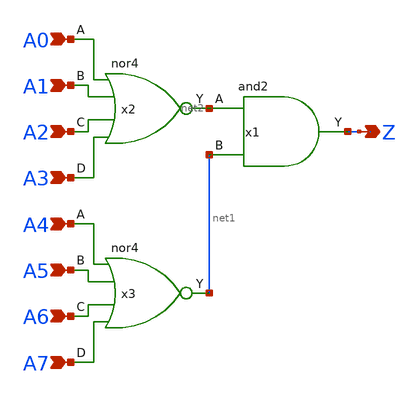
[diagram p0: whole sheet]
** sch_path: design/xschem/ZV_FLAG/Z_FLAG.sch
**.subckt Z_FLAG A0 A1 A2 A3 A4 A5 A6 A7 Z
*.ipin A0
*.ipin A1
*.ipin A2
*.ipin A3
*.ipin A4
*.ipin A5
*.ipin A6
*.ipin A7
*.opin Z
x2 A0 A1 A2 A3 VSS VDD net2 nor4
x3 A4 A5 A6 A7 VSS VDD net1 nor4
x1 net2 net1 VSS VDD Z and2
**.ends

* expanding   symbol:  NOR/nor4.sym # of pins=5
** sym_path: design/xschem/NOR/nor4.sym
** sch_path: design/xschem/NOR/nor4.sch
.subckt nor4 A B C D VSS VDD Y
*.ipin A
*.opin Y
*.ipin B
*.ipin C
*.ipin D
XM1 Y A net1 net1 sky130_fd_pr__pfet_01v8 L=0.15 W=12.8 nf=1 ad='int((nf+1)/2) * W/nf * 0.29' as='int((nf+2)/2) * W/nf * 0.29'
+ pd='2*int((nf+1)/2) * (W/nf + 0.29)' ps='2*int((nf+2)/2) * (W/nf + 0.29)' nrd='0.29 / W' nrs='0.29 / W'
+ sa=0 sb=0 sd=0 mult=1 m=1
XM2 Y A VSS VSS sky130_fd_pr__nfet_01v8 L=0.15 W=1 nf=1 ad='int((nf+1)/2) * W/nf * 0.29' as='int((nf+2)/2) * W/nf * 0.29'
+ pd='2*int((nf+1)/2) * (W/nf + 0.29)' ps='2*int((nf+2)/2) * (W/nf + 0.29)' nrd='0.29 / W' nrs='0.29 / W'
+ sa=0 sb=0 sd=0 mult=1 m=1
XM3 Y B VSS VSS sky130_fd_pr__nfet_01v8 L=0.15 W=1 nf=1 ad='int((nf+1)/2) * W/nf * 0.29' as='int((nf+2)/2) * W/nf * 0.29'
+ pd='2*int((nf+1)/2) * (W/nf + 0.29)' ps='2*int((nf+2)/2) * (W/nf + 0.29)' nrd='0.29 / W' nrs='0.29 / W'
+ sa=0 sb=0 sd=0 mult=1 m=1
XM4 net1 B net3 net3 sky130_fd_pr__pfet_01v8 L=0.15 W=12.8 nf=1 ad='int((nf+1)/2) * W/nf * 0.29' as='int((nf+2)/2) * W/nf * 0.29'
+ pd='2*int((nf+1)/2) * (W/nf + 0.29)' ps='2*int((nf+2)/2) * (W/nf + 0.29)' nrd='0.29 / W' nrs='0.29 / W'
+ sa=0 sb=0 sd=0 mult=1 m=1
XM5 net3 C net2 net2 sky130_fd_pr__pfet_01v8 L=0.15 W=12.8 nf=1 ad='int((nf+1)/2) * W/nf * 0.29' as='int((nf+2)/2) * W/nf * 0.29'
+ pd='2*int((nf+1)/2) * (W/nf + 0.29)' ps='2*int((nf+2)/2) * (W/nf + 0.29)' nrd='0.29 / W' nrs='0.29 / W'
+ sa=0 sb=0 sd=0 mult=1 m=1
XM6 Y C VSS VSS sky130_fd_pr__nfet_01v8 L=0.15 W=1 nf=1 ad='int((nf+1)/2) * W/nf * 0.29' as='int((nf+2)/2) * W/nf * 0.29'
+ pd='2*int((nf+1)/2) * (W/nf + 0.29)' ps='2*int((nf+2)/2) * (W/nf + 0.29)' nrd='0.29 / W' nrs='0.29 / W'
+ sa=0 sb=0 sd=0 mult=1 m=1
XM7 Y D VSS VSS sky130_fd_pr__nfet_01v8 L=0.15 W=1 nf=1 ad='int((nf+1)/2) * W/nf * 0.29' as='int((nf+2)/2) * W/nf * 0.29'
+ pd='2*int((nf+1)/2) * (W/nf + 0.29)' ps='2*int((nf+2)/2) * (W/nf + 0.29)' nrd='0.29 / W' nrs='0.29 / W'
+ sa=0 sb=0 sd=0 mult=1 m=1
XM8 net2 D VDD VDD sky130_fd_pr__pfet_01v8 L=0.15 W=12.8 nf=1 ad='int((nf+1)/2) * W/nf * 0.29' as='int((nf+2)/2) * W/nf * 0.29'
+ pd='2*int((nf+1)/2) * (W/nf + 0.29)' ps='2*int((nf+2)/2) * (W/nf + 0.29)' nrd='0.29 / W' nrs='0.29 / W'
+ sa=0 sb=0 sd=0 mult=1 m=1
.ends


* expanding   symbol:  AND/and2.sym # of pins=3
** sym_path: design/xschem/AND/and2.sym
** sch_path: design/xschem/AND/and2.sch
.subckt and2 A B VSS VDD Y
*.ipin A
*.ipin B
*.opin Y
x1 net1 VSS VDD Y inv
x2 A B VSS VDD net1 nand2
.ends


* expanding   symbol:  INV/inv.sym # of pins=2
** sym_path: design/xschem/INV/inv.sym
** sch_path: design/xschem/INV/inv.sch
.subckt inv A VSS VDD Y
*.ipin A
*.opin Y
XM2 Y A VSS GND sky130_fd_pr__nfet_01v8 L=0.15 W=1 nf=1 ad='int((nf+1)/2) * W/nf * 0.29' as='int((nf+2)/2) * W/nf * 0.29'
+ pd='2*int((nf+1)/2) * (W/nf + 0.29)' ps='2*int((nf+2)/2) * (W/nf + 0.29)' nrd='0.29 / W' nrs='0.29 / W'
+ sa=0 sb=0 sd=0 mult=1 m=1
XM1 Y A VDD VDD sky130_fd_pr__pfet_01v8 L=0.15 W=3.21 nf=1 ad='int((nf+1)/2) * W/nf * 0.29' as='int((nf+2)/2) * W/nf * 0.29'
+ pd='2*int((nf+1)/2) * (W/nf + 0.29)' ps='2*int((nf+2)/2) * (W/nf + 0.29)' nrd='0.29 / W' nrs='0.29 / W'
+ sa=0 sb=0 sd=0 mult=1 m=1
.ends


* expanding   symbol:  NAND/nand2.sym # of pins=3
** sym_path: design/xschem/NAND/nand2.sym
** sch_path: design/xschem/NAND/nand2.sch
.subckt nand2 A B VSS VDD Y
*.ipin A
*.opin Y
*.ipin B
XM1 Y A VDD VDD sky130_fd_pr__pfet_01v8 L=0.15 W=3.2 nf=1 ad='int((nf+1)/2) * W/nf * 0.29' as='int((nf+2)/2) * W/nf * 0.29'
+ pd='2*int((nf+1)/2) * (W/nf + 0.29)' ps='2*int((nf+2)/2) * (W/nf + 0.29)' nrd='0.29 / W' nrs='0.29 / W'
+ sa=0 sb=0 sd=0 mult=1 m=1
XM2 Y A net1 net1 sky130_fd_pr__nfet_01v8 L=0.15 W=2 nf=1 ad='int((nf+1)/2) * W/nf * 0.29' as='int((nf+2)/2) * W/nf * 0.29'
+ pd='2*int((nf+1)/2) * (W/nf + 0.29)' ps='2*int((nf+2)/2) * (W/nf + 0.29)' nrd='0.29 / W' nrs='0.29 / W'
+ sa=0 sb=0 sd=0 mult=1 m=1
XM3 net1 B VSS VSS sky130_fd_pr__nfet_01v8 L=0.15 W=2 nf=1 ad='int((nf+1)/2) * W/nf * 0.29' as='int((nf+2)/2) * W/nf * 0.29'
+ pd='2*int((nf+1)/2) * (W/nf + 0.29)' ps='2*int((nf+2)/2) * (W/nf + 0.29)' nrd='0.29 / W' nrs='0.29 / W'
+ sa=0 sb=0 sd=0 mult=1 m=1
XM4 Y B VDD VDD sky130_fd_pr__pfet_01v8 L=0.15 W=3.2 nf=1 ad='int((nf+1)/2) * W/nf * 0.29' as='int((nf+2)/2) * W/nf * 0.29'
+ pd='2*int((nf+1)/2) * (W/nf + 0.29)' ps='2*int((nf+2)/2) * (W/nf + 0.29)' nrd='0.29 / W' nrs='0.29 / W'
+ sa=0 sb=0 sd=0 mult=1 m=1
.ends

.end
